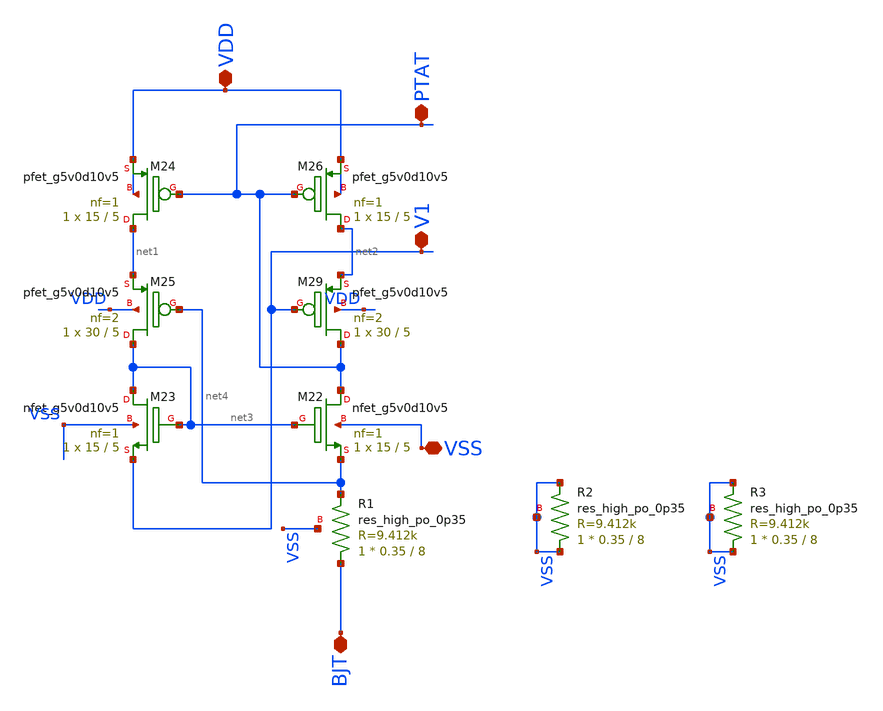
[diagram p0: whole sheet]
** sch_path: xschem/xschem_BGR_Top/PTAT.sch
**.subckt PTAT VDD PTAT V1 BJT VSS
*.iopin VDD
*.iopin PTAT
*.iopin V1
*.iopin BJT
*.iopin VSS
XM22 PTAT net3 net4 VSS sky130_fd_pr__nfet_g5v0d10v5 L=5 W=15 nf=1 ad='int((nf+1)/2) * W/nf * 0.29' as='int((nf+2)/2) * W/nf * 0.29'
+ pd='2*int((nf+1)/2) * (W/nf + 0.29)' ps='2*int((nf+2)/2) * (W/nf + 0.29)' nrd='0.29 / W' nrs='0.29 / W'
+ sa=0 sb=0 sd=0 mult=1 m=1
XM23 net3 net3 V1 VSS sky130_fd_pr__nfet_g5v0d10v5 L=5 W=15 nf=1 ad='int((nf+1)/2) * W/nf * 0.29' as='int((nf+2)/2) * W/nf * 0.29'
+ pd='2*int((nf+1)/2) * (W/nf + 0.29)' ps='2*int((nf+2)/2) * (W/nf + 0.29)' nrd='0.29 / W' nrs='0.29 / W'
+ sa=0 sb=0 sd=0 mult=1 m=1
XM24 net1 PTAT VDD VDD sky130_fd_pr__pfet_g5v0d10v5 L=5 W=15 nf=1 ad='int((nf+1)/2) * W/nf * 0.29' as='int((nf+2)/2) * W/nf * 0.29'
+ pd='2*int((nf+1)/2) * (W/nf + 0.29)' ps='2*int((nf+2)/2) * (W/nf + 0.29)' nrd='0.29 / W' nrs='0.29 / W'
+ sa=0 sb=0 sd=0 mult=1 m=1
XM25 net3 net4 net1 VDD sky130_fd_pr__pfet_g5v0d10v5 L=5 W=30 nf=2 ad='int((nf+1)/2) * W/nf * 0.29' as='int((nf+2)/2) * W/nf * 0.29'
+ pd='2*int((nf+1)/2) * (W/nf + 0.29)' ps='2*int((nf+2)/2) * (W/nf + 0.29)' nrd='0.29 / W' nrs='0.29 / W'
+ sa=0 sb=0 sd=0 mult=1 m=1
XM26 net2 PTAT VDD VDD sky130_fd_pr__pfet_g5v0d10v5 L=5 W=15 nf=1 ad='int((nf+1)/2) * W/nf * 0.29' as='int((nf+2)/2) * W/nf * 0.29'
+ pd='2*int((nf+1)/2) * (W/nf + 0.29)' ps='2*int((nf+2)/2) * (W/nf + 0.29)' nrd='0.29 / W' nrs='0.29 / W'
+ sa=0 sb=0 sd=0 mult=1 m=1
XM29 PTAT V1 net2 VDD sky130_fd_pr__pfet_g5v0d10v5 L=5 W=30 nf=2 ad='int((nf+1)/2) * W/nf * 0.29' as='int((nf+2)/2) * W/nf * 0.29'
+ pd='2*int((nf+1)/2) * (W/nf + 0.29)' ps='2*int((nf+2)/2) * (W/nf + 0.29)' nrd='0.29 / W' nrs='0.29 / W'
+ sa=0 sb=0 sd=0 mult=1 m=1
XR1 BJT net4 VSS sky130_fd_pr__res_high_po_0p35 L=8 mult=1 m=1
XR2 VSS VSS VSS sky130_fd_pr__res_high_po_0p35 L=8 mult=1 m=1
XR3 VSS VSS VSS sky130_fd_pr__res_high_po_0p35 L=8 mult=1 m=1
**.ends
.end
